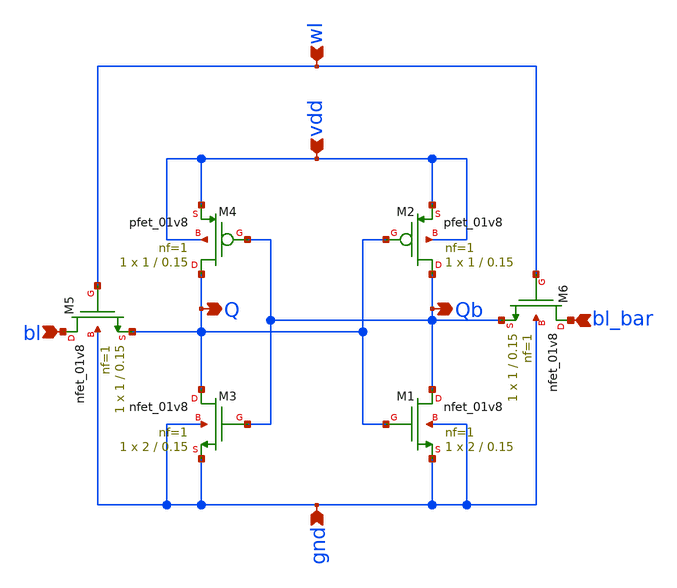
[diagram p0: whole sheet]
** sch_path: Projects/Schematic_Design_and_Analysis_of_an_8-Word_8-Bit_Static_RAM_with_6T_Storage_Cells_using_SKY130PDK/assets/schematic/sram_6t_cell.sch
**.subckt sram_6t_cell gnd vdd bl_bar bl wl Q Qb
*.ipin gnd
*.ipin vdd
*.ipin bl_bar
*.ipin bl
*.ipin wl
*.opin Q
*.opin Qb
XM1 Qb Q gnd gnd sky130_fd_pr__nfet_01v8 L=0.15 W=2 nf=1 ad='int((nf+1)/2) * W/nf * 0.29' as='int((nf+2)/2) * W/nf * 0.29'
+ pd='2*int((nf+1)/2) * (W/nf + 0.29)' ps='2*int((nf+2)/2) * (W/nf + 0.29)' nrd='0.29 / W' nrs='0.29 / W'
+ sa=0 sb=0 sd=0 mult=1 m=1
XM2 Qb Q vdd vdd sky130_fd_pr__pfet_01v8 L=0.15 W=1 nf=1 ad='int((nf+1)/2) * W/nf * 0.29' as='int((nf+2)/2) * W/nf * 0.29'
+ pd='2*int((nf+1)/2) * (W/nf + 0.29)' ps='2*int((nf+2)/2) * (W/nf + 0.29)' nrd='0.29 / W' nrs='0.29 / W'
+ sa=0 sb=0 sd=0 mult=1 m=1
XM3 Q Qb gnd gnd sky130_fd_pr__nfet_01v8 L=0.15 W=2 nf=1 ad='int((nf+1)/2) * W/nf * 0.29' as='int((nf+2)/2) * W/nf * 0.29'
+ pd='2*int((nf+1)/2) * (W/nf + 0.29)' ps='2*int((nf+2)/2) * (W/nf + 0.29)' nrd='0.29 / W' nrs='0.29 / W'
+ sa=0 sb=0 sd=0 mult=1 m=1
XM4 Q Qb vdd vdd sky130_fd_pr__pfet_01v8 L=0.15 W=1 nf=1 ad='int((nf+1)/2) * W/nf * 0.29' as='int((nf+2)/2) * W/nf * 0.29'
+ pd='2*int((nf+1)/2) * (W/nf + 0.29)' ps='2*int((nf+2)/2) * (W/nf + 0.29)' nrd='0.29 / W' nrs='0.29 / W'
+ sa=0 sb=0 sd=0 mult=1 m=1
XM5 bl wl Q gnd sky130_fd_pr__nfet_01v8 L=0.15 W=1 nf=1 ad='int((nf+1)/2) * W/nf * 0.29' as='int((nf+2)/2) * W/nf * 0.29'
+ pd='2*int((nf+1)/2) * (W/nf + 0.29)' ps='2*int((nf+2)/2) * (W/nf + 0.29)' nrd='0.29 / W' nrs='0.29 / W'
+ sa=0 sb=0 sd=0 mult=1 m=1
XM6 bl_bar wl Qb gnd sky130_fd_pr__nfet_01v8 L=0.15 W=1 nf=1 ad='int((nf+1)/2) * W/nf * 0.29' as='int((nf+2)/2) * W/nf * 0.29'
+ pd='2*int((nf+1)/2) * (W/nf + 0.29)' ps='2*int((nf+2)/2) * (W/nf + 0.29)' nrd='0.29 / W' nrs='0.29 / W'
+ sa=0 sb=0 sd=0 mult=1 m=1
**.ends
.end
